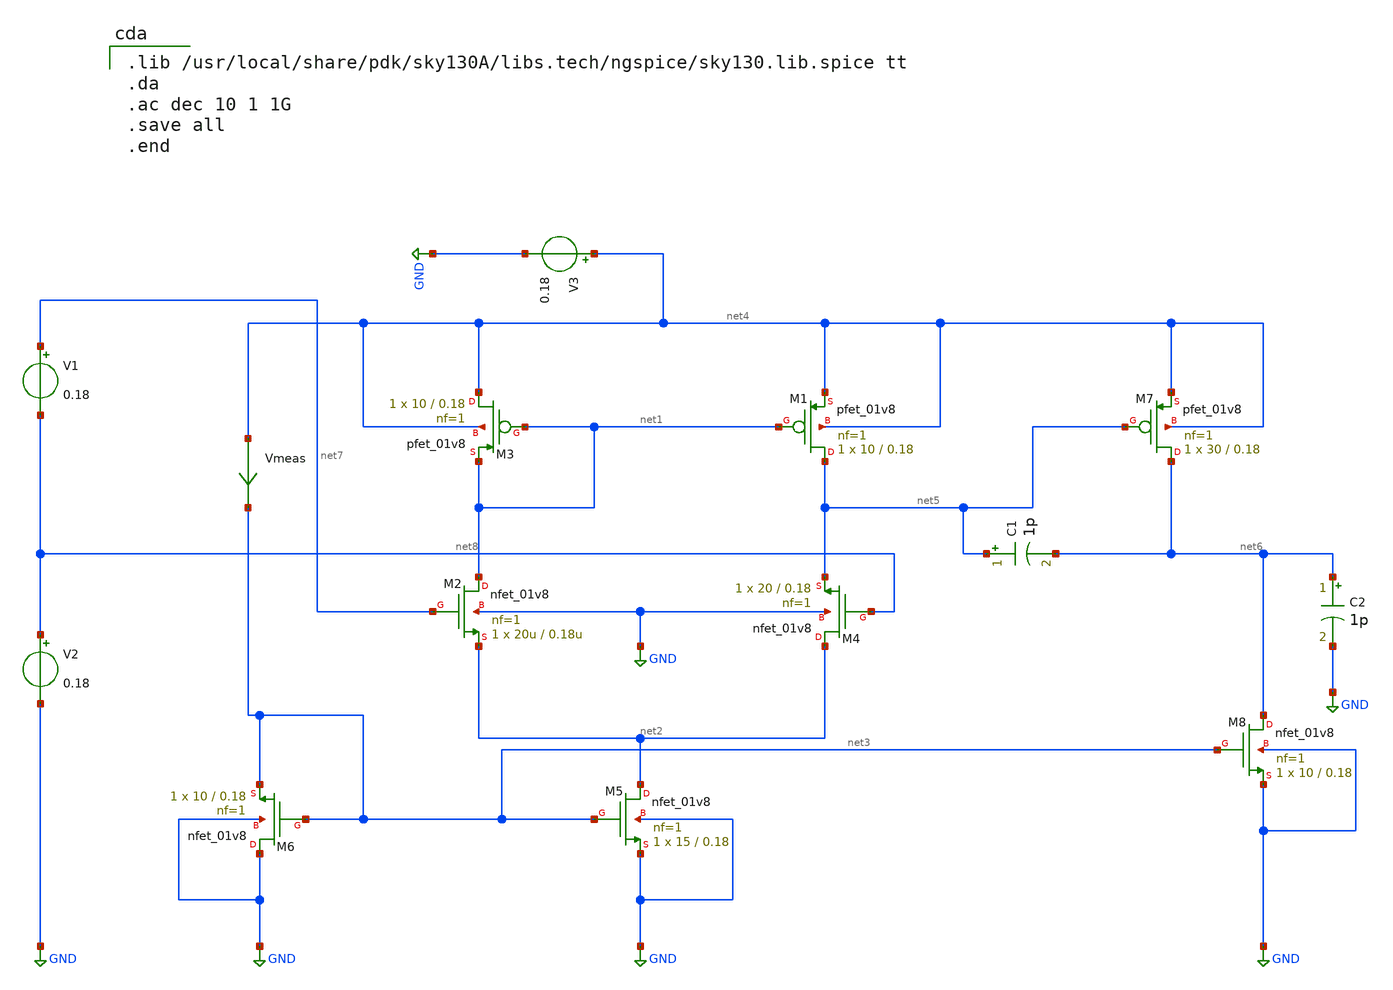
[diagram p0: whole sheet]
** sch_path: operationalapmlifier.sch
**.subckt operationalapmlifier
XM1 net5 net1 net4 net4 sky130_fd_pr__pfet_01v8 L=0.18 W=10 nf=1 ad='int((1 + 1)/2) * 10 / 1 * 0.29'
+ as='int((1 + 2)/2) * 10 / 1 * 0.29' pd='2*int((1 + 1)/2) * (10 / 1 + 0.29)' ps='2*int((1 + 2)/2) * (10 / 1 + 0.29)'
+ nrd='0.29 / 10 ' nrs='0.29 / 10 ' sa=0 sb=0 sd=0 mult=1 m=1
XM2 net1 net7 net2 GND sky130_fd_pr__nfet_01v8 L=0.18u W=20u nf=1 ad='int((1 + 1)/2) * 20u / 1 * 0.29'
+ as='int((1 + 2)/2) * 20u / 1 * 0.29' pd='2*int((1 + 1)/2) * (20u / 1 + 0.29)' ps='2*int((1 + 2)/2) * (20u / 1 + 0.29)'
+ nrd='0.29 / 20u ' nrs='0.29 / 20u ' sa=0 sb=0 sd=0 mult=1 m=1
XM3 net4 net1 net1 net4 sky130_fd_pr__pfet_01v8 L=0.18 W=10 nf=1 ad='int((1 + 1)/2) * 10 / 1 * 0.29'
+ as='int((1 + 2)/2) * 10 / 1 * 0.29' pd='2*int((1 + 1)/2) * (10 / 1 + 0.29)' ps='2*int((1 + 2)/2) * (10 / 1 + 0.29)'
+ nrd='0.29 / 10 ' nrs='0.29 / 10 ' sa=0 sb=0 sd=0 mult=1 m=1
XM4 net2 net8 net5 GND sky130_fd_pr__nfet_01v8 L=0.18 W=20 nf=1 ad='int((1 + 1)/2) * 20 / 1 * 0.29' as='int((1 + 2)/2) * 20 / 1 * 0.29'
+ pd='2*int((1 + 1)/2) * (20 / 1 + 0.29)' ps='2*int((1 + 2)/2) * (20 / 1 + 0.29)' nrd='0.29 / 20 ' nrs='0.29 / 20 '
+ sa=0 sb=0 sd=0 mult=1 m=1
XM5 net2 net3 GND GND sky130_fd_pr__nfet_01v8 L=0.18 W=15 nf=1 ad='int((1 + 1)/2) * 15 / 1 * 0.29' as='int((1 + 2)/2) * 15 / 1 * 0.29'
+ pd='2*int((1 + 1)/2) * (15 / 1 + 0.29)' ps='2*int((1 + 2)/2) * (15 / 1 + 0.29)' nrd='0.29 / 15 ' nrs='0.29 / 15 '
+ sa=0 sb=0 sd=0 mult=1 m=1
XM6 GND net3 net3 GND sky130_fd_pr__nfet_01v8 L=0.18 W=10 nf=1 ad='int((1 + 1)/2) * 10 / 1 * 0.29' as='int((1 + 2)/2) * 10 / 1 * 0.29'
+ pd='2*int((1 + 1)/2) * (10 / 1 + 0.29)' ps='2*int((1 + 2)/2) * (10 / 1 + 0.29)' nrd='0.29 / 10 ' nrs='0.29 / 10 '
+ sa=0 sb=0 sd=0 mult=1 m=1
XM7 net6 net5 net4 net4 sky130_fd_pr__pfet_01v8 L=0.18 W=30 nf=1 ad='int((1 + 1)/2) * 30 / 1 * 0.29'
+ as='int((1 + 2)/2) * 30 / 1 * 0.29' pd='2*int((1 + 1)/2) * (30 / 1 + 0.29)' ps='2*int((1 + 2)/2) * (30 / 1 + 0.29)'
+ nrd='0.29 / 30 ' nrs='0.29 / 30 ' sa=0 sb=0 sd=0 mult=1 m=1
XM8 net6 net3 GND GND sky130_fd_pr__nfet_01v8 L=0.18 W=10 nf=1 ad='int((1 + 1)/2) * 10 / 1 * 0.29' as='int((1 + 2)/2) * 10 / 1 * 0.29'
+ pd='2*int((1 + 1)/2) * (10 / 1 + 0.29)' ps='2*int((1 + 2)/2) * (10 / 1 + 0.29)' nrd='0.29 / 10 ' nrs='0.29 / 10 '
+ sa=0 sb=0 sd=0 mult=1 m=1
V1 net7 net8 0.18
Vmeas net4 net3 0
.save i(vmeas)
C1 net5 net6 1p m=1
V2 net8 GND 0.18
C2 net6 GND 1p m=1
V3 net4 GND 0.18
**** begin user architecture code

.lib /usr/local/share/pdk/sky130A/libs.tech/ngspice/sky130.lib.spice tt
.da
.ac dec 10 1 1G
.save all
.end

vout
**** end user architecture code
**.ends
.GLOBAL GND
.end
